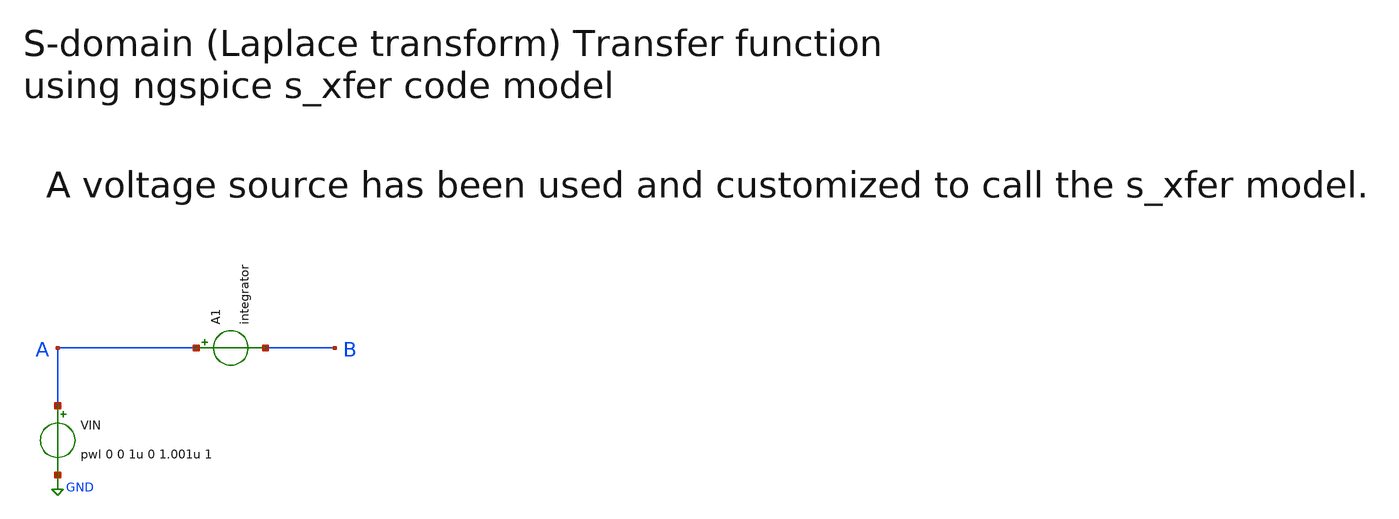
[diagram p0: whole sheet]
** sch_path: sky130A/xschem_libs/sky130_tests_ase/test_s_xfer/schematic/test_s_xfer.sch
* Copyright 2021 Stefan Frederik Schippers
* Licensed under the Apache License, Version 2.0 (the "License");
* you may not use this file except in compliance with the License.
* You may obtain a copy of the License at
* https://www.apache.org/licenses/LICENSE-2.0
* Unless required by applicable law or agreed to in writing, software
* distributed under the License is distributed on an "AS IS" BASIS,
* WITHOUT WARRANTIES OR CONDITIONS OF ANY KIND, either express or implied.
* See the License for the specific language governing permissions and
* limitations under the License.
**.subckt test_s_xfer
A1 A B integrator
VIN A GND pwl 0 0 1u 0 1.001u 1
**.ends
.GLOBAL GND
**** begin user architecture code

.model integrator s_xfer(num_coeff=[1] den_coeff=[1 0] int_ic=[0] denormalized_freq=1e5)

**** end user architecture code
.end
